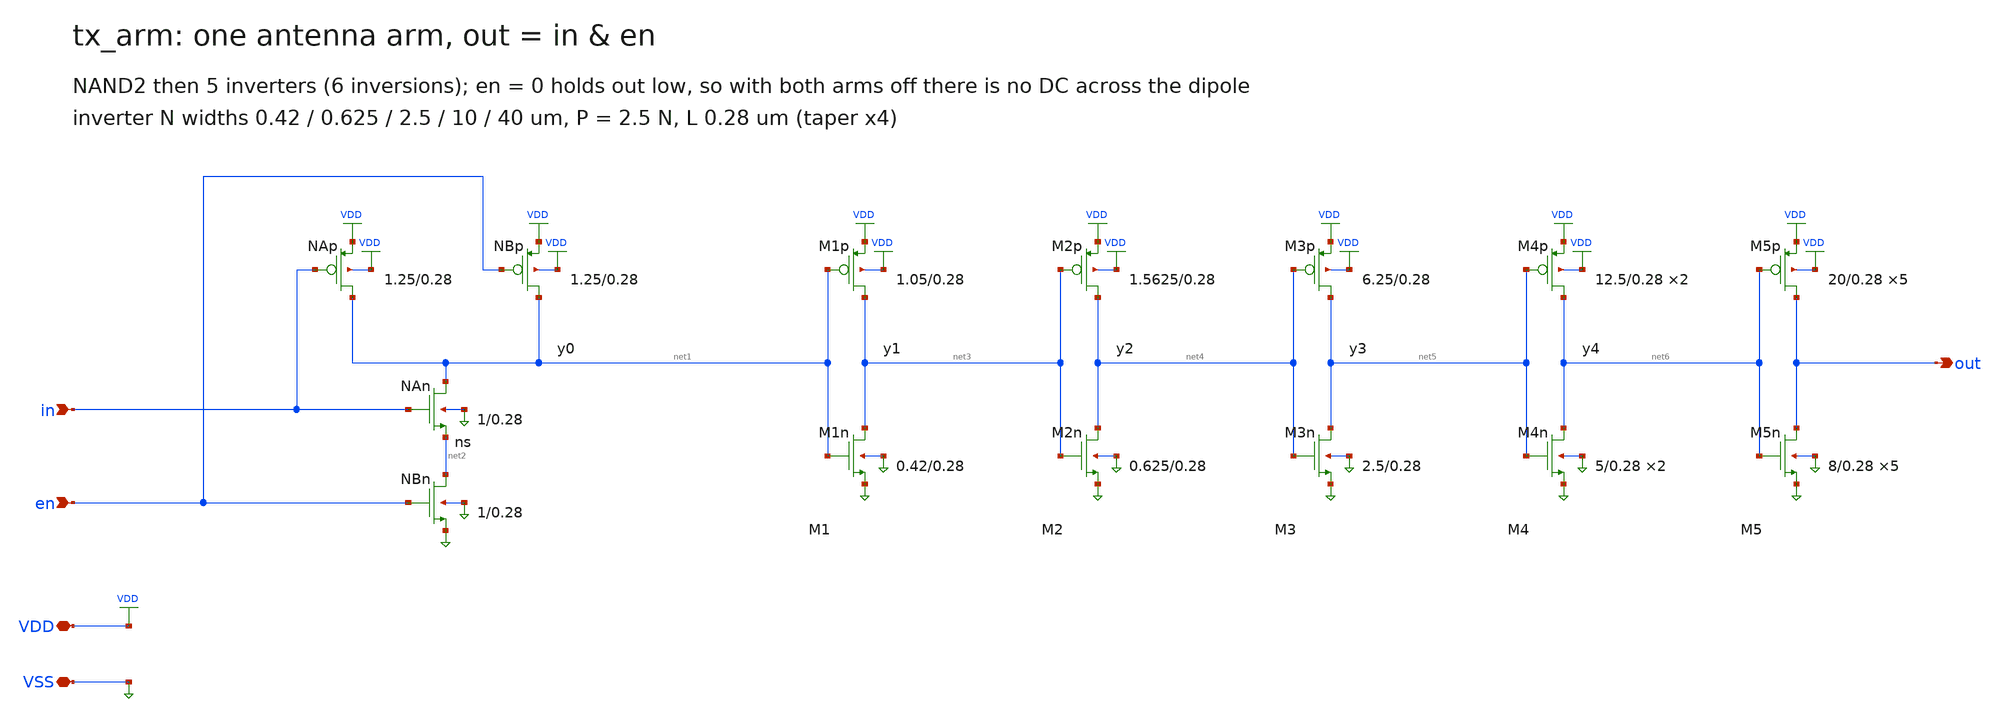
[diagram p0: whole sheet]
** sch_path: xschem/tx_arm.sch
**.subckt tx_arm VDD VSS in en out
*.iopin VDD
*.iopin VSS
*.ipin in
*.ipin en
*.opin out
XNAp net1 in VDD VDD pfet_03v3 L=0.28u W=1.25u nf=1 ad=0.625p as=0.625p pd=3.5u ps=3.5u nrd=0 nrs=0
+ sa=0 sb=0 sd=0 m=1
XNBp net1 en VDD VDD pfet_03v3 L=0.28u W=1.25u nf=1 ad=0.625p as=0.625p pd=3.5u ps=3.5u nrd=0 nrs=0
+ sa=0 sb=0 sd=0 m=1
XNAn net1 in net2 VSS nfet_03v3 L=0.28u W=1.0u nf=1 ad=0.5p as=0.5p pd=3.0u ps=3.0u nrd=0 nrs=0 sa=0
+ sb=0 sd=0 m=1
XNBn net2 en VSS VSS nfet_03v3 L=0.28u W=1.0u nf=1 ad=0.5p as=0.5p pd=3.0u ps=3.0u nrd=0 nrs=0 sa=0
+ sb=0 sd=0 m=1
XM1p net3 net1 VDD VDD pfet_03v3 L=0.28u W=1.0499999999999998u nf=1 ad=0.5249999999999999p
+ as=0.5249999999999999p pd=3.0999999999999996u ps=3.0999999999999996u nrd=0 nrs=0 sa=0 sb=0 sd=0 m=1
XM1n net3 net1 VSS VSS nfet_03v3 L=0.28u W=0.41999999999999993u nf=1 ad=0.20999999999999996p
+ as=0.20999999999999996p pd=1.8399999999999999u ps=1.8399999999999999u nrd=0 nrs=0 sa=0 sb=0 sd=0 m=1
XM2p net4 net3 VDD VDD pfet_03v3 L=0.28u W=1.5624999999999998u nf=1 ad=0.7812499999999999p
+ as=0.7812499999999999p pd=4.125u ps=4.125u nrd=0 nrs=0 sa=0 sb=0 sd=0 m=1
XM2n net4 net3 VSS VSS nfet_03v3 L=0.28u W=0.625u nf=1 ad=0.3125p as=0.3125p pd=2.25u ps=2.25u nrd=0
+ nrs=0 sa=0 sb=0 sd=0 m=1
XM3p net5 net4 VDD VDD pfet_03v3 L=0.28u W=6.249999999999999u nf=1 ad=3.1249999999999996p
+ as=3.1249999999999996p pd=13.499999999999998u ps=13.499999999999998u nrd=0 nrs=0 sa=0 sb=0 sd=0 m=1
XM3n net5 net4 VSS VSS nfet_03v3 L=0.28u W=2.5u nf=1 ad=1.25p as=1.25p pd=6.0u ps=6.0u nrd=0 nrs=0
+ sa=0 sb=0 sd=0 m=1
XM4p net6 net5 VDD VDD pfet_03v3 L=0.28u W=12.499999999999998u nf=1 ad=6.249999999999999p
+ as=6.249999999999999p pd=25.999999999999996u ps=25.999999999999996u nrd=0 nrs=0 sa=0 sb=0 sd=0 m=2
XM4n net6 net5 VSS VSS nfet_03v3 L=0.28u W=5.0u nf=1 ad=2.5p as=2.5p pd=11.0u ps=11.0u nrd=0 nrs=0
+ sa=0 sb=0 sd=0 m=2
XM5p out net6 VDD VDD pfet_03v3 L=0.28u W=20.0u nf=1 ad=10.0p as=10.0p pd=41.0u ps=41.0u nrd=0 nrs=0
+ sa=0 sb=0 sd=0 m=5
XM5n out net6 VSS VSS nfet_03v3 L=0.28u W=8.0u nf=1 ad=4.0p as=4.0p pd=17.0u ps=17.0u nrd=0 nrs=0
+ sa=0 sb=0 sd=0 m=5
**.ends
.end
